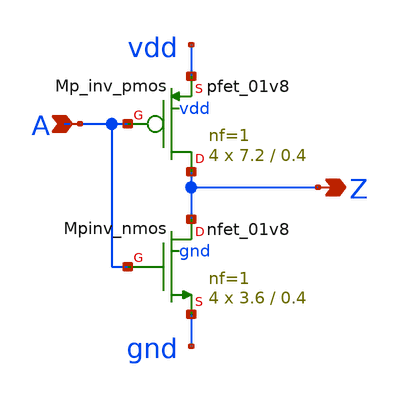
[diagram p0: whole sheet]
** sch_path: sram_4_16_scn4m/pinv_8.sch
**.subckt pinv_8 A Z
*.ipin A
*.opin Z
XMpinv_nmos Z A gnd gnd sky130_fd_pr__nfet_01v8 L=0.4 W=3.6 nf=1 ad='int((nf+1)/2) * W/nf * 0.29' as='int((nf+2)/2) * W/nf * 0.29'
+ pd='2*int((nf+1)/2) * (W/nf + 0.29)' ps='2*int((nf+2)/2) * (W/nf + 0.29)' nrd='0.29 / W' nrs='0.29 / W'
+ sa=0 sb=0 sd=0 mult=4 m=4
XMp_inv_pmos Z A vdd vdd sky130_fd_pr__pfet_01v8 L=0.4 W=7.2 nf=1 ad='int((nf+1)/2) * W/nf * 0.29' as='int((nf+2)/2) * W/nf * 0.29'
+ pd='2*int((nf+1)/2) * (W/nf + 0.29)' ps='2*int((nf+2)/2) * (W/nf + 0.29)' nrd='0.29 / W' nrs='0.29 / W'
+ sa=0 sb=0 sd=0 mult=4 m=4
**.ends
.end
